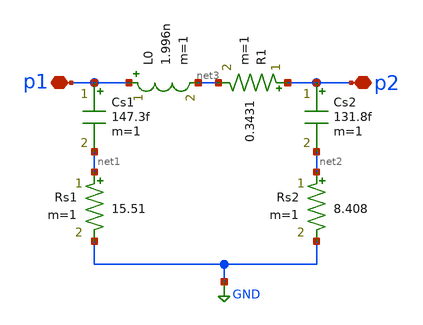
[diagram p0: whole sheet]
** sch_path: xschem-2.45GHz/l1-2.45G.sch
**.subckt l1-2.45G p2 p1
*.iopin p2
*.iopin p1
L0 p1 net3 1.996n m=1
Cs1 p1 net1 147.3f m=1
Cs2 p2 net2 131.8f m=1
Rs1 net1 GND 15.51 m=1
Rs2 net2 GND 8.408 m=1
R1 p2 net3 0.3431 m=1
**.ends
.GLOBAL GND
.end
